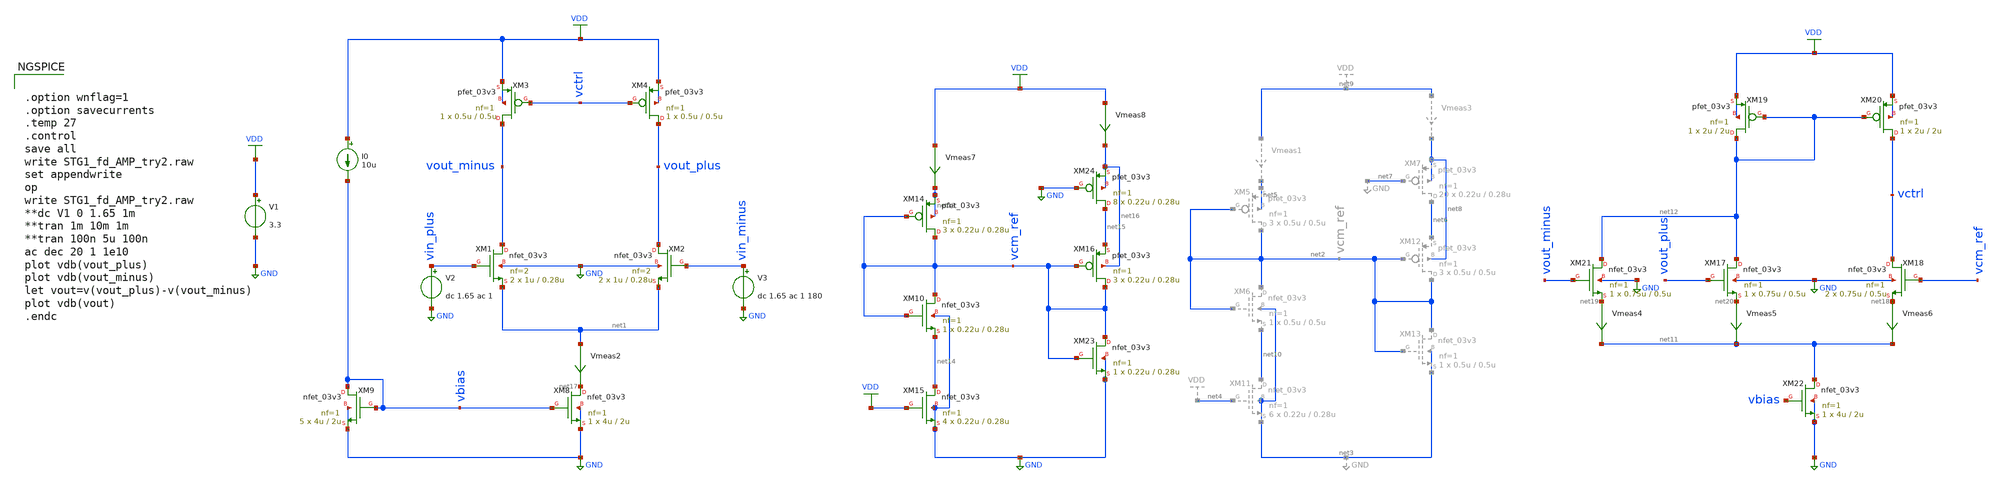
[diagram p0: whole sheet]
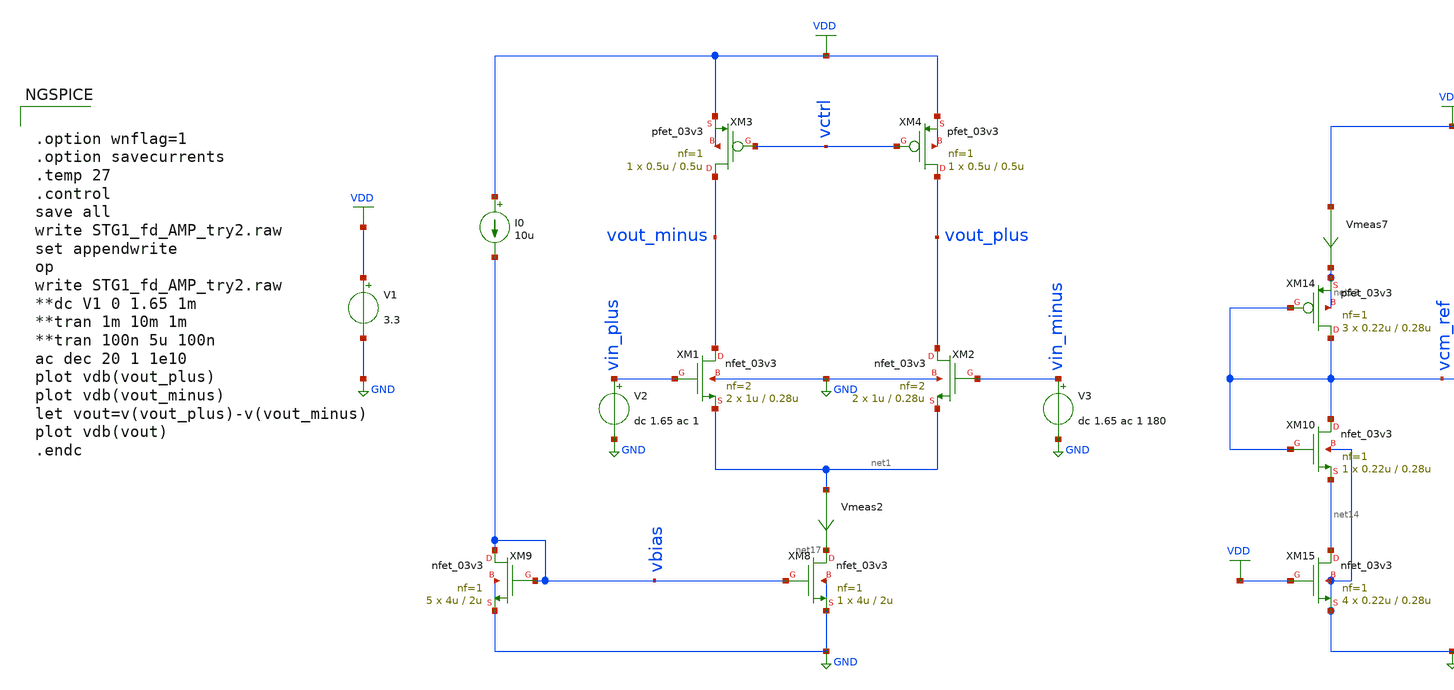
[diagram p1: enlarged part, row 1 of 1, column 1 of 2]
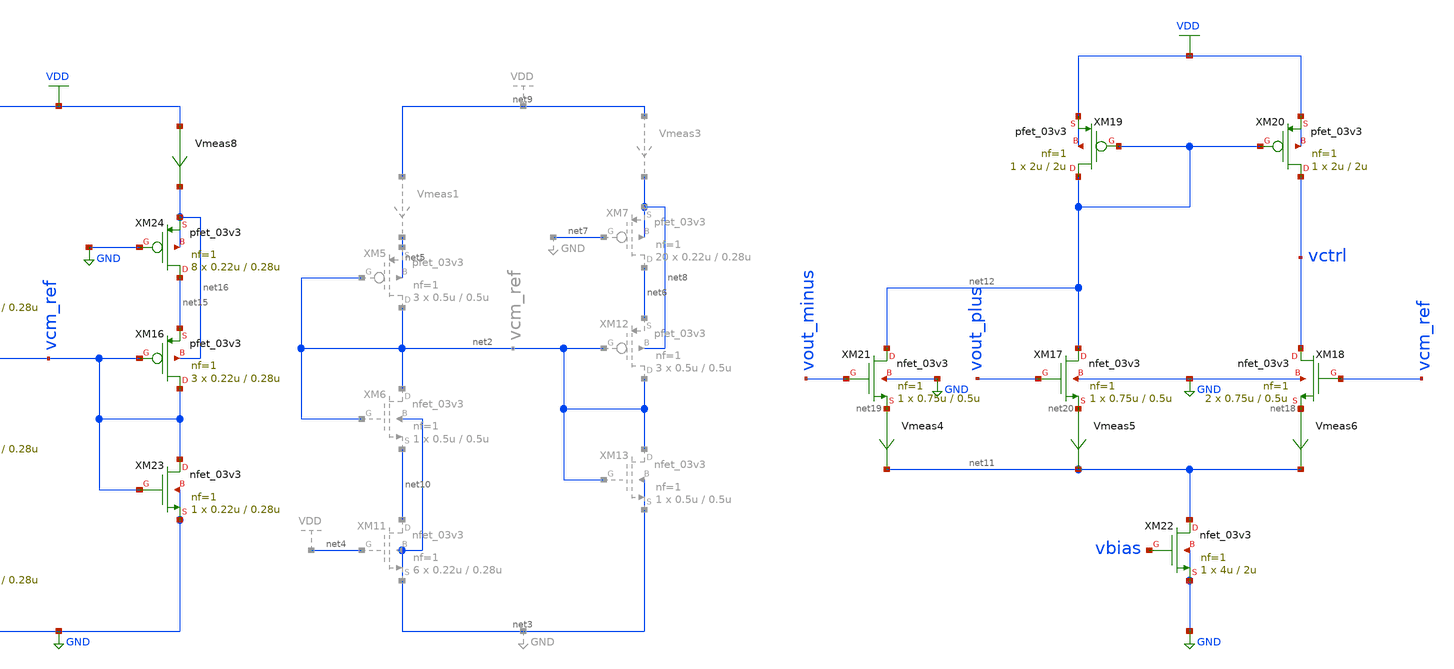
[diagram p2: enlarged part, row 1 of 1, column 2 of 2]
** sch_path: Design_Files/Ring-amp/STG1/STG1_fd_AMP_try2.sch
**.subckt STG1_fd_AMP_try2
XM1 vout_minus vin_plus net1 GND nfet_03v3 L=0.28u W=1u nf=2 ad='int((nf+1)/2) * W/nf * 0.18u' as='int((nf+2)/2) * W/nf * 0.18u'
+ pd='2*int((nf+1)/2) * (W/nf + 0.18u)' ps='2*int((nf+2)/2) * (W/nf + 0.18u)' nrd='0.18u / W' nrs='0.18u / W'
+ sa=0 sb=0 sd=0 m=2
XM3 vout_minus vctrl VDD VDD pfet_03v3 L=0.5u W=0.5u nf=1 ad='int((nf+1)/2) * W/nf * 0.18u' as='int((nf+2)/2) * W/nf * 0.18u'
+ pd='2*int((nf+1)/2) * (W/nf + 0.18u)' ps='2*int((nf+2)/2) * (W/nf + 0.18u)' nrd='0.18u / W' nrs='0.18u / W'
+ sa=0 sb=0 sd=0 m=1
V2 vin_plus GND dc 1.65 ac 1
XM8 net17 vbias GND GND nfet_03v3 L=2u W=4u nf=1 ad='int((nf+1)/2) * W/nf * 0.18u' as='int((nf+2)/2) * W/nf * 0.18u'
+ pd='2*int((nf+1)/2) * (W/nf + 0.18u)' ps='2*int((nf+2)/2) * (W/nf + 0.18u)' nrd='0.18u / W' nrs='0.18u / W'
+ sa=0 sb=0 sd=0 m=1
Vmeas2 net1 net17 0
.save i(vmeas2)
V3 vin_minus GND dc 1.65 ac 1 180
XM9 vbias vbias GND GND nfet_03v3 L=2u W=4u nf=1 ad='int((nf+1)/2) * W/nf * 0.18u' as='int((nf+2)/2) * W/nf * 0.18u'
+ pd='2*int((nf+1)/2) * (W/nf + 0.18u)' ps='2*int((nf+2)/2) * (W/nf + 0.18u)' nrd='0.18u / W' nrs='0.18u / W'
+ sa=0 sb=0 sd=0 m=5
I0 VDD vbias 10u
XM2 vout_plus vin_minus net1 GND nfet_03v3 L=0.28u W=1u nf=2 ad='int((nf+1)/2) * W/nf * 0.18u' as='int((nf+2)/2) * W/nf * 0.18u'
+ pd='2*int((nf+1)/2) * (W/nf + 0.18u)' ps='2*int((nf+2)/2) * (W/nf + 0.18u)' nrd='0.18u / W' nrs='0.18u / W'
+ sa=0 sb=0 sd=0 m=2
XM4 vout_plus vctrl VDD VDD pfet_03v3 L=0.5u W=0.5u nf=1 ad='int((nf+1)/2) * W/nf * 0.18u' as='int((nf+2)/2) * W/nf * 0.18u'
+ pd='2*int((nf+1)/2) * (W/nf + 0.18u)' ps='2*int((nf+2)/2) * (W/nf + 0.18u)' nrd='0.18u / W' nrs='0.18u / W'
+ sa=0 sb=0 sd=0 m=1
XM18 vctrl vcm_ref net18 GND nfet_03v3 L=0.5u W=0.75u nf=1 ad='int((nf+1)/2) * W/nf * 0.18u' as='int((nf+2)/2) * W/nf * 0.18u'
+ pd='2*int((nf+1)/2) * (W/nf + 0.18u)' ps='2*int((nf+2)/2) * (W/nf + 0.18u)' nrd='0.18u / W' nrs='0.18u / W'
+ sa=0 sb=0 sd=0 m=2
XM19 net12 net12 VDD VDD pfet_03v3 L=2u W=2u nf=1 ad='int((nf+1)/2) * W/nf * 0.18u' as='int((nf+2)/2) * W/nf * 0.18u'
+ pd='2*int((nf+1)/2) * (W/nf + 0.18u)' ps='2*int((nf+2)/2) * (W/nf + 0.18u)' nrd='0.18u / W' nrs='0.18u / W'
+ sa=0 sb=0 sd=0 m=1
XM20 vctrl net12 VDD VDD pfet_03v3 L=2u W=2u nf=1 ad='int((nf+1)/2) * W/nf * 0.18u' as='int((nf+2)/2) * W/nf * 0.18u'
+ pd='2*int((nf+1)/2) * (W/nf + 0.18u)' ps='2*int((nf+2)/2) * (W/nf + 0.18u)' nrd='0.18u / W' nrs='0.18u / W'
+ sa=0 sb=0 sd=0 m=1
XM21 net12 vout_minus net19 GND nfet_03v3 L=0.5u W=0.75u nf=1 ad='int((nf+1)/2) * W/nf * 0.18u' as='int((nf+2)/2) * W/nf * 0.18u'
+ pd='2*int((nf+1)/2) * (W/nf + 0.18u)' ps='2*int((nf+2)/2) * (W/nf + 0.18u)' nrd='0.18u / W' nrs='0.18u / W'
+ sa=0 sb=0 sd=0 m=1
XM22 net11 vbias GND GND nfet_03v3 L=2u W=4u nf=1 ad='int((nf+1)/2) * W/nf * 0.18u' as='int((nf+2)/2) * W/nf * 0.18u'
+ pd='2*int((nf+1)/2) * (W/nf + 0.18u)' ps='2*int((nf+2)/2) * (W/nf + 0.18u)' nrd='0.18u / W' nrs='0.18u / W'
+ sa=0 sb=0 sd=0 m=1
V1 VDD GND 3.3
XM17 net12 vout_plus net20 GND nfet_03v3 L=0.5u W=0.75u nf=1 ad='int((nf+1)/2) * W/nf * 0.18u' as='int((nf+2)/2) * W/nf * 0.18u'
+ pd='2*int((nf+1)/2) * (W/nf + 0.18u)' ps='2*int((nf+2)/2) * (W/nf + 0.18u)' nrd='0.18u / W' nrs='0.18u / W'
+ sa=0 sb=0 sd=0 m=1
Vmeas4 net19 net11 0
.save i(vmeas4)
Vmeas5 net20 net11 0
.save i(vmeas5)
Vmeas6 net18 net11 0
.save i(vmeas6)
XM10 vcm_ref vcm_ref net14 GND nfet_03v3 L=0.28u W=0.22u nf=1 ad='int((nf+1)/2) * W/nf * 0.18u' as='int((nf+2)/2) * W/nf * 0.18u'
+ pd='2*int((nf+1)/2) * (W/nf + 0.18u)' ps='2*int((nf+2)/2) * (W/nf + 0.18u)' nrd='0.18u / W' nrs='0.18u / W'
+ sa=0 sb=0 sd=0 m=1
XM14 vcm_ref vcm_ref net13 net13 pfet_03v3 L=0.28u W=0.22u nf=1 ad='int((nf+1)/2) * W/nf * 0.18u' as='int((nf+2)/2) * W/nf * 0.18u'
+ pd='2*int((nf+1)/2) * (W/nf + 0.18u)' ps='2*int((nf+2)/2) * (W/nf + 0.18u)' nrd='0.18u / W' nrs='0.18u / W'
+ sa=0 sb=0 sd=0 m=3
XM15 net14 VDD GND GND nfet_03v3 L=0.28u W=0.22u nf=1 ad='int((nf+1)/2) * W/nf * 0.18u' as='int((nf+2)/2) * W/nf * 0.18u'
+ pd='2*int((nf+1)/2) * (W/nf + 0.18u)' ps='2*int((nf+2)/2) * (W/nf + 0.18u)' nrd='0.18u / W' nrs='0.18u / W'
+ sa=0 sb=0 sd=0 m=4
Vmeas7 VDD net13 0
.save i(vmeas7)
XM16 vcm_ref vcm_ref net15 net16 pfet_03v3 L=0.28u W=0.22u nf=1 ad='int((nf+1)/2) * W/nf * 0.18u' as='int((nf+2)/2) * W/nf * 0.18u'
+ pd='2*int((nf+1)/2) * (W/nf + 0.18u)' ps='2*int((nf+2)/2) * (W/nf + 0.18u)' nrd='0.18u / W' nrs='0.18u / W'
+ sa=0 sb=0 sd=0 m=3
XM23 vcm_ref vcm_ref GND GND nfet_03v3 L=0.28u W=0.22u nf=1 ad='int((nf+1)/2) * W/nf * 0.18u' as='int((nf+2)/2) * W/nf * 0.18u'
+ pd='2*int((nf+1)/2) * (W/nf + 0.18u)' ps='2*int((nf+2)/2) * (W/nf + 0.18u)' nrd='0.18u / W' nrs='0.18u / W'
+ sa=0 sb=0 sd=0 m=1
XM24 net15 GND net16 net16 pfet_03v3 L=0.28u W=0.22u nf=1 ad='int((nf+1)/2) * W/nf * 0.18u' as='int((nf+2)/2) * W/nf * 0.18u'
+ pd='2*int((nf+1)/2) * (W/nf + 0.18u)' ps='2*int((nf+2)/2) * (W/nf + 0.18u)' nrd='0.18u / W' nrs='0.18u / W'
+ sa=0 sb=0 sd=0 m=8
Vmeas8 VDD net16 0
.save i(vmeas8)
**** begin user architecture code


.option wnflag=1
.option savecurrents
.temp 27
.control
save all
write STG1_fd_AMP_try2.raw
set appendwrite
op
write STG1_fd_AMP_try2.raw
**dc V1 0 1.65 1m
**tran 1m 10m 1m
**tran 100n 5u 100n
ac dec 20 1 1e10
plot vdb(vout_plus)
plot vdb(vout_minus)
let vout=v(vout_plus)-v(vout_minus)
plot vdb(vout)
.endc




.save @m.xm1.m0[gm]
.save @m.xm1.m0[id]
.save @m.xm1.m0[vth]
.save @m.xm1.m0[vds]
.save @m.xm1.m0[gds]
.save @m.xm1.m0[cgg]
.save @m.xm1.m0[cgs]
.save @m.xm1.m0[cgd]
.save @m.xm2.m0[gm]
.save @m.xm2.m0[id]
.save @m.xm2.m0[vth]
.save @m.xm2.m0[vds]
.save @m.xm2.m0[gds]
.save @m.xm2.m0[cgg]
.save @m.xm2.m0[cgs]
.save @m.xm2.m0[cgd]
.save @m.xm3.m0[gm]
.save @m.xm3.m0[id]
.save @m.xm3.m0[vth]
.save @m.xm3.m0[vds]
.save @m.xm3.m0[gds]
.save @m.xm3.m0[cgg]
.save @m.xm3.m0[cgs]
.save @m.xm3.m0[cgd]
.save @m.xm4.m0[gm]
.save @m.xm4.m0[id]
.save @m.xm4.m0[vth]
.save @m.xm4.m0[vds]
.save @m.xm4.m0[gds]
.save @m.xm4.m0[cgg]
.save @m.xm4.m0[cgs]
.save @m.xm4.m0[cgd]
.save @m.xm5.m0[gm]
.save @m.xm5.m0[id]
.save @m.xm5.m0[vth]
.save @m.xm5.m0[vds]
.save @m.xm5.m0[gds]
.save @m.xm5.m0[cgg]
.save @m.xm5.m0[cgs]
.save @m.xm5.m0[cgd]
.save @m.xm6.m0[gm]
.save @m.xm6.m0[id]
.save @m.xm6.m0[vth]
.save @m.xm6.m0[vds]
.save @m.xm6.m0[gds]
.save @m.xm6.m0[cgg]
.save @m.xm6.m0[cgs]
.save @m.xm6.m0[cgd]
.save @m.xm7.m0[gm]
.save @m.xm7.m0[id]
.save @m.xm7.m0[vth]
.save @m.xm7.m0[vds]
.save @m.xm7.m0[gds]
.save @m.xm7.m0[cgg]
.save @m.xm7.m0[cgs]
.save @m.xm7.m0[cgd]
.save @m.xm8.m0[gm]
.save @m.xm8.m0[id]
.save @m.xm8.m0[vth]
.save @m.xm8.m0[vds]
.save @m.xm8.m0[gds]
.save @m.xm8.m0[cgg]
.save @m.xm8.m0[cgs]
.save @m.xm8.m0[cgd]
.save @m.xm9.m0[gm]
.save @m.xm9.m0[id]
.save @m.xm9.m0[vth]
.save @m.xm9.m0[vds]
.save @m.xm9.m0[gds]
.save @m.xm9.m0[cgg]
.save @m.xm9.m0[cgs]
.save @m.xm9.m0[cgd]
.save @m.xm10.m0[gm]
.save @m.xm10.m0[id]
.save @m.xm10.m0[vth]
.save @m.xm10.m0[vds]
.save @m.xm10.m0[gds]
.save @m.xm10.m0[cgg]
.save @m.xm10.m0[cgs]
.save @m.xm10.m0[cgd]
.save @m.xm11.m0[gm]
.save @m.xm11.m0[id]
.save @m.xm11.m0[vth]
.save @m.xm11.m0[vds]
.save @m.xm11.m0[gds]
.save @m.xm11.m0[cgg]
.save @m.xm11.m0[cgs]
.save @m.xm11.m0[cgd]
.save @m.xm12.m0[gm]
.save @m.xm12.m0[id]
.save @m.xm12.m0[vth]
.save @m.xm12.m0[vds]
.save @m.xm12.m0[gds]
.save @m.xm12.m0[cgg]
.save @m.xm12.m0[cgs]
.save @m.xm12.m0[cgd]
.save @m.xm13.m0[gm]
.save @m.xm13.m0[id]
.save @m.xm13.m0[vth]
.save @m.xm13.m0[vds]
.save @m.xm13.m0[gds]
.save @m.xm13.m0[cgg]
.save @m.xm13.m0[cgs]
.save @m.xm13.m0[cgd]
.save @m.xm14.m0[gm]
.save @m.xm14.m0[id]
.save @m.xm14.m0[vth]
.save @m.xm14.m0[vds]
.save @m.xm14.m0[gds]
.save @m.xm14.m0[cgg]
.save @m.xm14.m0[cgs]
.save @m.xm14.m0[cgd]
.save @m.xm15.m0[gm]
.save @m.xm15.m0[id]
.save @m.xm15.m0[vth]
.save @m.xm15.m0[vds]
.save @m.xm15.m0[gds]
.save @m.xm15.m0[cgg]
.save @m.xm15.m0[cgs]
.save @m.xm15.m0[cgd]
.save @m.xm16.m0[gm]
.save @m.xm16.m0[id]
.save @m.xm16.m0[vth]
.save @m.xm16.m0[vds]
.save @m.xm16.m0[gds]
.save @m.xm16.m0[cgg]
.save @m.xm16.m0[cgs]
.save @m.xm16.m0[cgd]
.save @m.xm17.m0[gm]
.save @m.xm17.m0[id]
.save @m.xm17.m0[vth]
.save @m.xm17.m0[vds]
.save @m.xm17.m0[gds]
.save @m.xm17.m0[cgg]
.save @m.xm17.m0[cgs]
.save @m.xm17.m0[cgd]
.save @m.xm18.m0[gm]
.save @m.xm18.m0[id]
.save @m.xm18.m0[vth]
.save @m.xm18.m0[vds]
.save @m.xm18.m0[gds]
.save @m.xm18.m0[cgg]
.save @m.xm18.m0[cgs]
.save @m.xm18.m0[cgd]
.save @m.xm19.m0[gm]
.save @m.xm19.m0[id]
.save @m.xm19.m0[vth]
.save @m.xm19.m0[vds]
.save @m.xm19.m0[gds]
.save @m.xm19.m0[cgg]
.save @m.xm19.m0[cgs]
.save @m.xm19.m0[cgd]
.save @m.xm20.m0[gm]
.save @m.xm20.m0[id]
.save @m.xm20.m0[vth]
.save @m.xm20.m0[vds]
.save @m.xm20.m0[gds]
.save @m.xm20.m0[cgg]
.save @m.xm20.m0[cgs]
.save @m.xm20.m0[cgd]
.save @m.xm21.m0[gm]
.save @m.xm21.m0[id]
.save @m.xm21.m0[vth]
.save @m.xm21.m0[vds]
.save @m.xm21.m0[gds]
.save @m.xm21.m0[cgg]
.save @m.xm21.m0[cgs]
.save @m.xm21.m0[cgd]
.save @m.xm22.m0[gm]
.save @m.xm22.m0[id]
.save @m.xm22.m0[vth]
.save @m.xm22.m0[vds]
.save @m.xm22.m0[gds]
.save @m.xm22.m0[cgg]
.save @m.xm22.m0[cgs]
.save @m.xm22.m0[cgd]



.lib /foss/pdks/volare/gf180mcu/versions/0fe599b2afb6708d281543108caf8310912f54af/gf180mcuD/libs.tech/ngspice/sm141064.ngspice typical
.include /foss/pdks/volare/gf180mcu/versions/0fe599b2afb6708d281543108caf8310912f54af/gf180mcuD/libs.tech/ngspice/design.ngspice
.lib /foss/pdks/volare/gf180mcu/versions/0fe599b2afb6708d281543108caf8310912f54af/gf180mcuD/libs.tech/ngspice/sm141064.ngspice res_statistical

**.include $::180MCU_MODELS/design.ngspice
**.lib $::180MCU_MODELS/sm141064.ngspice typical
**.lib $::180MCU_MODELS/sm141064.ngspice res_typical
* .lib $::180MCU_MODELS/sm141064.ngspice res_statistical
*.include $::180MCU_MODELS/design.ngspice
*.lib $::180MCU_MODELS/sm141064.ngspice typical


**** end user architecture code
**.ends
.GLOBAL VDD
.GLOBAL GND
.end
